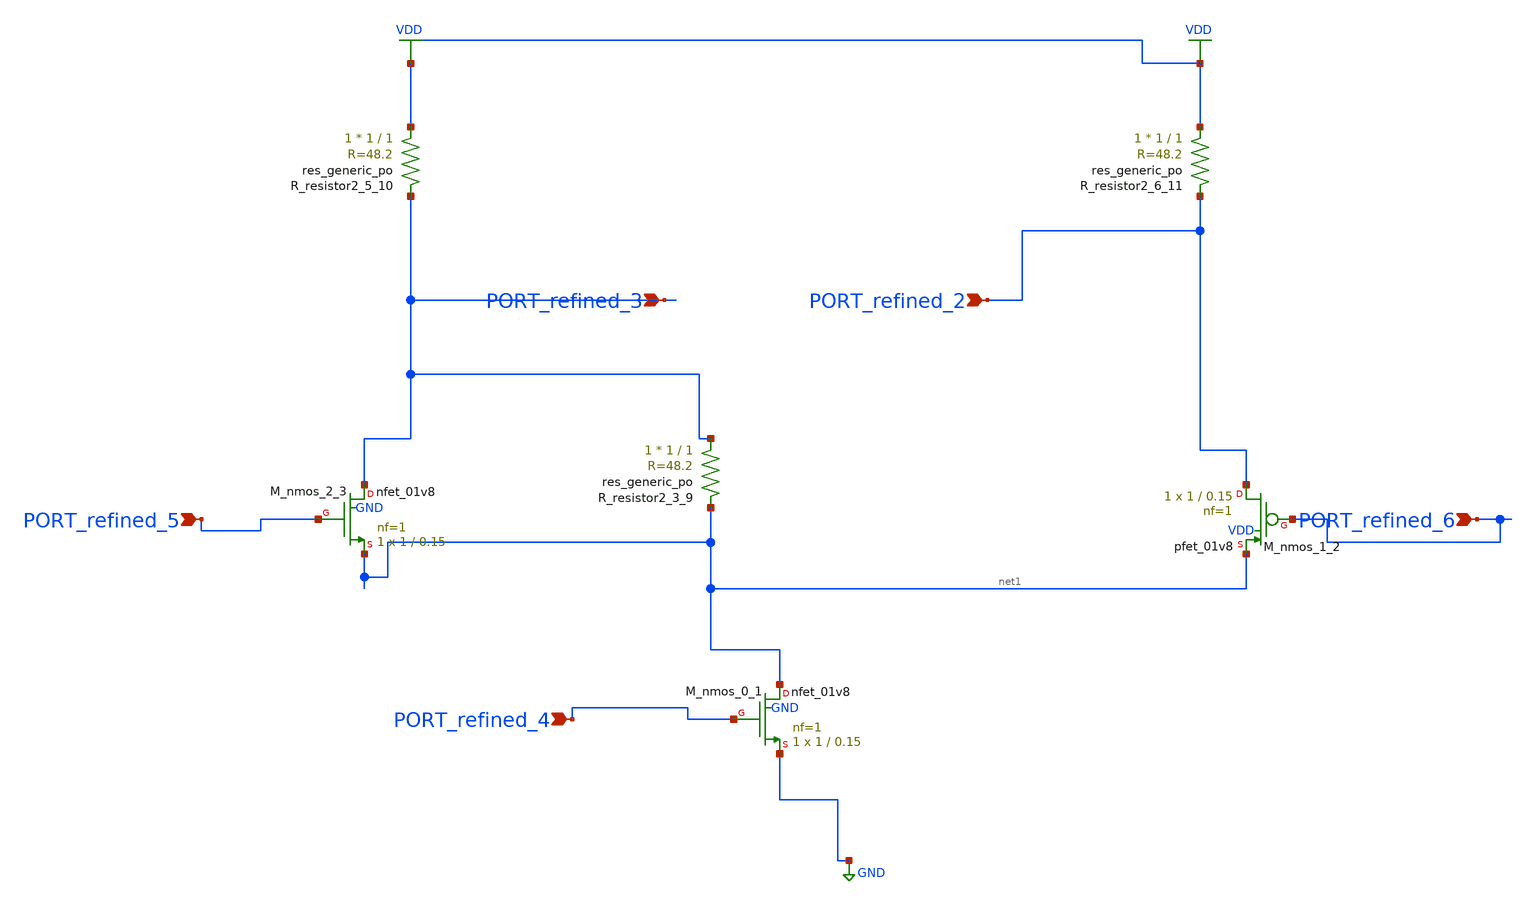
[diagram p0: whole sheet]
** sch_path: schematics/AMSNet/248.sch
**.subckt 248 PORT_refined_2 PORT_refined_3 PORT_refined_4 PORT_refined_5 PORT_refined_6
*.ipin PORT_refined_2
*.ipin PORT_refined_3
*.ipin PORT_refined_4
*.ipin PORT_refined_5
*.ipin PORT_refined_6
XM_nmos_0_1 net1 PORT_refined_4 GND GND sky130_fd_pr__nfet_01v8 L=0.15 W=1 nf=1 ad='int((1 + 1)/2) * 1 / 1 * 0.29'
+ as='int((1 + 2)/2) * 1 / 1 * 0.29' pd='2*int((1 + 1)/2) * (1 / 1 + 0.29)' ps='2*int((1 + 2)/2) * (1 / 1 + 0.29)'
+ nrd='0.29 / 1 ' nrs='0.29 / 1 ' sa=0 sb=0 sd=0 mult=1 m=1
XM_nmos_1_2 PORT_refined_2 PORT_refined_6 net1 VDD sky130_fd_pr__pfet_01v8 L=0.15 W=1 nf=1 ad='int((1 + 1)/2) * 1 / 1 * 0.29'
+ as='int((1 + 2)/2) * 1 / 1 * 0.29' pd='2*int((1 + 1)/2) * (1 / 1 + 0.29)' ps='2*int((1 + 2)/2) * (1 / 1 + 0.29)'
+ nrd='0.29 / 1 ' nrs='0.29 / 1 ' sa=0 sb=0 sd=0 mult=1 m=1
XM_nmos_2_3 PORT_refined_3 PORT_refined_5 net1 GND sky130_fd_pr__nfet_01v8 L=0.15 W=1 nf=1 ad='int((1 + 1)/2) * 1 / 1 * 0.29'
+ as='int((1 + 2)/2) * 1 / 1 * 0.29' pd='2*int((1 + 1)/2) * (1 / 1 + 0.29)' ps='2*int((1 + 2)/2) * (1 / 1 + 0.29)'
+ nrd='0.29 / 1 ' nrs='0.29 / 1 ' sa=0 sb=0 sd=0 mult=1 m=1
XR_resistor2_3_9 PORT_refined_3 net1 sky130_fd_pr__res_generic_po W=1 L=1 m=1
XR_resistor2_5_10 VDD PORT_refined_3 sky130_fd_pr__res_generic_po W=1 L=1 m=1
XR_resistor2_6_11 VDD PORT_refined_2 sky130_fd_pr__res_generic_po W=1 L=1 m=1
**.ends
.GLOBAL GND
.GLOBAL VDD
.end
